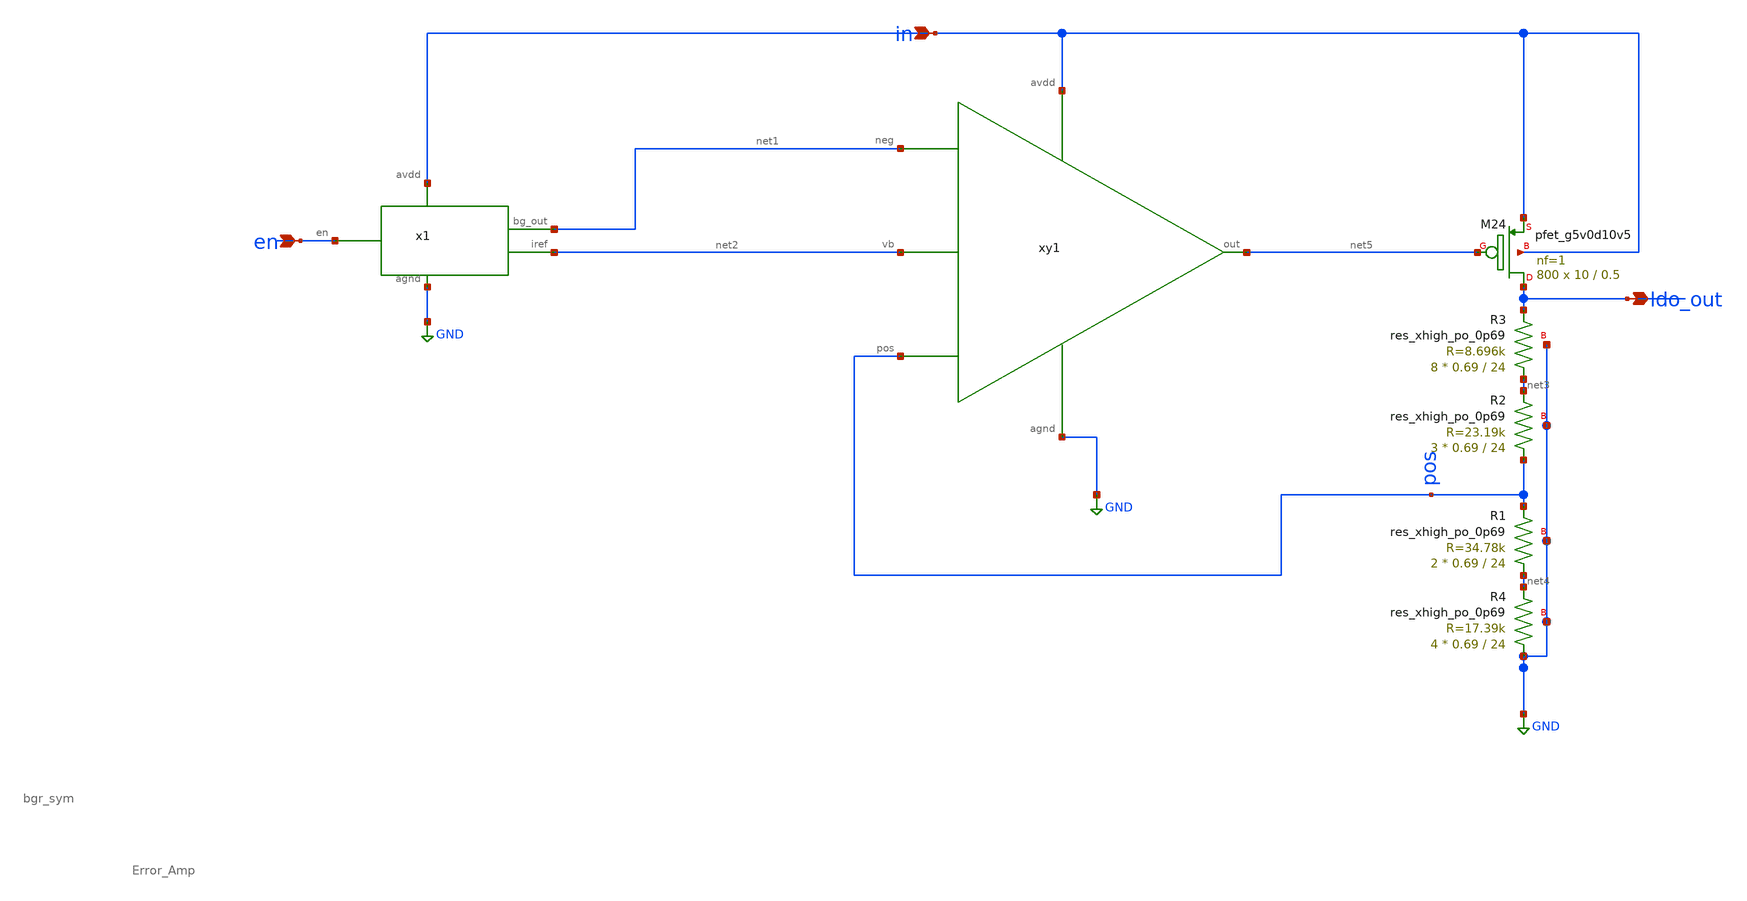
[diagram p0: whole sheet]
** sch_path: xschem/ldo_v1/ldo_v1_lvs.sch
**.subckt ldo_v1_lvs in en ldo_out
*.ipin in
*.ipin en
*.opin ldo_out
x1 in net1 GND net2 en bgr_sym
xy1 net1 pos net2 net5 in GND Error_Amp
XM24 ldo_out net5 in in sky130_fd_pr__pfet_g5v0d10v5 L=0.5 W=10 nf=1 ad='int((nf+1)/2) * W/nf * 0.29'
+ as='int((nf+2)/2) * W/nf * 0.29' pd='2*int((nf+1)/2) * (W/nf + 0.29)' ps='2*int((nf+2)/2) * (W/nf + 0.29)'
+ nrd='0.29 / W' nrs='0.29 / W' sa=0 sb=0 sd=0 mult=800 m=800
XR2 pos net3 GND sky130_fd_pr__res_xhigh_po_0p69 L=24 mult=3 m=3
XR3 net3 ldo_out GND sky130_fd_pr__res_xhigh_po_0p69 L=24 mult=8 m=8
XR1 net4 pos GND sky130_fd_pr__res_xhigh_po_0p69 L=24 mult=2 m=2
XR4 GND net4 GND sky130_fd_pr__res_xhigh_po_0p69 L=24 mult=4 m=4
**.ends

* expanding   symbol:  bgr_sym.sym # of pins=5
** sym_path: xschem/ldo_v1/bgr_sym.sym
** sch_path: xschem/ldo_v1/bgr_sym.sch
.subckt bgr_sym avdd bg_out agnd iref en
*.iopin avdd
*.iopin agnd
*.opin bg_out
*.opin iref
*.iopin en
XM2 iref mir avdd avdd sky130_fd_pr__pfet_g5v0d10v5 L=2 W=3 nf=1 ad='int((nf+1)/2) * W/nf * 0.29' as='int((nf+2)/2) * W/nf * 0.29'
+ pd='2*int((nf+1)/2) * (W/nf + 0.29)' ps='2*int((nf+2)/2) * (W/nf + 0.29)' nrd='0.29 / W' nrs='0.29 / W'
+ sa=0 sb=0 sd=0 mult=4 m=4
XM1 inn mir avdd avdd sky130_fd_pr__pfet_g5v0d10v5 L=2 W=3 nf=1 ad='int((nf+1)/2) * W/nf * 0.29' as='int((nf+2)/2) * W/nf * 0.29'
+ pd='2*int((nf+1)/2) * (W/nf + 0.29)' ps='2*int((nf+2)/2) * (W/nf + 0.29)' nrd='0.29 / W' nrs='0.29 / W'
+ sa=0 sb=0 sd=0 mult=8 m=8
XM3 inp mir avdd avdd sky130_fd_pr__pfet_g5v0d10v5 L=2 W=3 nf=1 ad='int((nf+1)/2) * W/nf * 0.29' as='int((nf+2)/2) * W/nf * 0.29'
+ pd='2*int((nf+1)/2) * (W/nf + 0.29)' ps='2*int((nf+2)/2) * (W/nf + 0.29)' nrd='0.29 / W' nrs='0.29 / W'
+ sa=0 sb=0 sd=0 mult=8 m=8
XM4 bg_out mir avdd avdd sky130_fd_pr__pfet_g5v0d10v5 L=2 W=3 nf=1 ad='int((nf+1)/2) * W/nf * 0.29' as='int((nf+2)/2) * W/nf * 0.29'
+ pd='2*int((nf+1)/2) * (W/nf + 0.29)' ps='2*int((nf+2)/2) * (W/nf + 0.29)' nrd='0.29 / W' nrs='0.29 / W'
+ sa=0 sb=0 sd=0 mult=8 m=8
XQ1 agnd agnd net2 sky130_fd_pr__pnp_05v5_W0p68L0p68 m=1
XQ5 agnd agnd net1 sky130_fd_pr__pnp_05v5_W0p68L0p68 m=1
XQ6 agnd agnd net1 sky130_fd_pr__pnp_05v5_W0p68L0p68 m=1
XQ7 agnd agnd net1 sky130_fd_pr__pnp_05v5_W0p68L0p68 m=1
XQ9 agnd agnd net1 sky130_fd_pr__pnp_05v5_W0p68L0p68 m=1
XQ11 agnd agnd net1 sky130_fd_pr__pnp_05v5_W0p68L0p68 m=1
XQ13 agnd agnd net1 sky130_fd_pr__pnp_05v5_W0p68L0p68 m=1
XQ15 agnd agnd net1 sky130_fd_pr__pnp_05v5_W0p68L0p68 m=1
XQ17 agnd agnd net1 sky130_fd_pr__pnp_05v5_W0p68L0p68 m=1
XM8 net4 net4 avdd avdd sky130_fd_pr__pfet_g5v0d10v5 L=2 W=3 nf=1 ad='int((nf+1)/2) * W/nf * 0.29' as='int((nf+2)/2) * W/nf * 0.29'
+ pd='2*int((nf+1)/2) * (W/nf + 0.29)' ps='2*int((nf+2)/2) * (W/nf + 0.29)' nrd='0.29 / W' nrs='0.29 / W'
+ sa=0 sb=0 sd=0 mult=4 m=4
XM12 net4 inp net3 agnd sky130_fd_pr__nfet_g5v0d10v5 L=1 W=3 nf=1 ad='int((nf+1)/2) * W/nf * 0.29' as='int((nf+2)/2) * W/nf * 0.29'
+ pd='2*int((nf+1)/2) * (W/nf + 0.29)' ps='2*int((nf+2)/2) * (W/nf + 0.29)' nrd='0.29 / W' nrs='0.29 / W'
+ sa=0 sb=0 sd=0 mult=8 m=8
XM21 mir inn net3 agnd sky130_fd_pr__nfet_g5v0d10v5 L=1 W=3 nf=1 ad='int((nf+1)/2) * W/nf * 0.29' as='int((nf+2)/2) * W/nf * 0.29'
+ pd='2*int((nf+1)/2) * (W/nf + 0.29)' ps='2*int((nf+2)/2) * (W/nf + 0.29)' nrd='0.29 / W' nrs='0.29 / W'
+ sa=0 sb=0 sd=0 mult=8 m=8
XM23 mir net4 avdd avdd sky130_fd_pr__pfet_g5v0d10v5 L=2 W=3 nf=1 ad='int((nf+1)/2) * W/nf * 0.29' as='int((nf+2)/2) * W/nf * 0.29'
+ pd='2*int((nf+1)/2) * (W/nf + 0.29)' ps='2*int((nf+2)/2) * (W/nf + 0.29)' nrd='0.29 / W' nrs='0.29 / W'
+ sa=0 sb=0 sd=0 mult=4 m=4
XM15 net3 net5 agnd agnd sky130_fd_pr__nfet_g5v0d10v5 L=2 W=5 nf=1 ad='int((nf+1)/2) * W/nf * 0.29' as='int((nf+2)/2) * W/nf * 0.29'
+ pd='2*int((nf+1)/2) * (W/nf + 0.29)' ps='2*int((nf+2)/2) * (W/nf + 0.29)' nrd='0.29 / W' nrs='0.29 / W'
+ sa=0 sb=0 sd=0 mult=4 m=4
XM25 net5 mir avdd avdd sky130_fd_pr__pfet_g5v0d10v5 L=2 W=3 nf=1 ad='int((nf+1)/2) * W/nf * 0.29' as='int((nf+2)/2) * W/nf * 0.29'
+ pd='2*int((nf+1)/2) * (W/nf + 0.29)' ps='2*int((nf+2)/2) * (W/nf + 0.29)' nrd='0.29 / W' nrs='0.29 / W'
+ sa=0 sb=0 sd=0 mult=8 m=8
XM16 net5 net5 agnd agnd sky130_fd_pr__nfet_g5v0d10v5 L=2 W=5 nf=1 ad='int((nf+1)/2) * W/nf * 0.29' as='int((nf+2)/2) * W/nf * 0.29'
+ pd='2*int((nf+1)/2) * (W/nf + 0.29)' ps='2*int((nf+2)/2) * (W/nf + 0.29)' nrd='0.29 / W' nrs='0.29 / W'
+ sa=0 sb=0 sd=0 mult=4 m=4
XR1 net6 inp agnd sky130_fd_pr__res_xhigh_po_0p69 L=27 mult=3 m=3
XR2 net2 inn agnd sky130_fd_pr__res_xhigh_po_0p69 L=27 mult=3 m=3
XR10 net1 net6 agnd sky130_fd_pr__res_xhigh_po_0p69 L=27 mult=6 m=6
XR11 agnd net7 agnd sky130_fd_pr__res_xhigh_po_0p69 L=27 mult=15 m=15
XR6 net10 net6 agnd sky130_fd_pr__res_xhigh_po_0p69 L=27 mult=1 m=1
XR5 net11 bg_out agnd sky130_fd_pr__res_xhigh_po_0p69 L=27 mult=1 m=1
XM19 mir en avdd avdd sky130_fd_pr__pfet_g5v0d10v5 L=0.5 W=0.42 nf=1 ad='int((nf+1)/2) * W/nf * 0.29'
+ as='int((nf+2)/2) * W/nf * 0.29' pd='2*int((nf+1)/2) * (W/nf + 0.29)' ps='2*int((nf+2)/2) * (W/nf + 0.29)'
+ nrd='0.29 / W' nrs='0.29 / W' sa=0 sb=0 sd=0 mult=2 m=2
XC2 avdd mir sky130_fd_pr__cap_mim_m3_1 W=20 L=20 MF=1 m=1
XM5 net9 net9 avdd avdd sky130_fd_pr__pfet_g5v0d10v5 L=3 W=0.42 nf=1 ad='int((nf+1)/2) * W/nf * 0.29'
+ as='int((nf+2)/2) * W/nf * 0.29' pd='2*int((nf+1)/2) * (W/nf + 0.29)' ps='2*int((nf+2)/2) * (W/nf + 0.29)'
+ nrd='0.29 / W' nrs='0.29 / W' sa=0 sb=0 sd=0 mult=2 m=2
XM6 net8 net8 net9 avdd sky130_fd_pr__pfet_g5v0d10v5 L=3 W=0.42 nf=1 ad='int((nf+1)/2) * W/nf * 0.29'
+ as='int((nf+2)/2) * W/nf * 0.29' pd='2*int((nf+1)/2) * (W/nf + 0.29)' ps='2*int((nf+2)/2) * (W/nf + 0.29)'
+ nrd='0.29 / W' nrs='0.29 / W' sa=0 sb=0 sd=0 mult=2 m=2
XM7 net8 bg_out agnd agnd sky130_fd_pr__nfet_g5v0d10v5 L=2 W=0.42 nf=1 ad='int((nf+1)/2) * W/nf * 0.29'
+ as='int((nf+2)/2) * W/nf * 0.29' pd='2*int((nf+1)/2) * (W/nf + 0.29)' ps='2*int((nf+2)/2) * (W/nf + 0.29)'
+ nrd='0.29 / W' nrs='0.29 / W' sa=0 sb=0 sd=0 mult=2 m=2
XM9 mir net8 agnd agnd sky130_fd_pr__nfet_g5v0d10v5 L=0.5 W=5 nf=1 ad='int((nf+1)/2) * W/nf * 0.29' as='int((nf+2)/2) * W/nf * 0.29'
+ pd='2*int((nf+1)/2) * (W/nf + 0.29)' ps='2*int((nf+2)/2) * (W/nf + 0.29)' nrd='0.29 / W' nrs='0.29 / W'
+ sa=0 sb=0 sd=0 mult=4 m=4
XR3 agnd net10 agnd sky130_fd_pr__res_xhigh_po_0p69 L=27 mult=15 m=15
XR4 agnd net11 agnd sky130_fd_pr__res_xhigh_po_0p69 L=27 mult=53 m=53
XR7 net7 net2 agnd sky130_fd_pr__res_xhigh_po_0p69 L=27 mult=1 m=1
.ends


* expanding   symbol:  Error_Amp.sym # of pins=6
** sym_path: xschem/ldo_v1/Error_Amp.sym
** sch_path: xschem/ldo_v1/Error_Amp.sch
.subckt Error_Amp neg pos vb out avdd agnd
*.opin out
*.iopin avdd
*.iopin agnd
*.iopin vb
*.ipin neg
*.ipin pos
XM8 net2 net2 avdd avdd sky130_fd_pr__pfet_g5v0d10v5 L=1.2 W=3 nf=1 ad='int((nf+1)/2) * W/nf * 0.29'
+ as='int((nf+2)/2) * W/nf * 0.29' pd='2*int((nf+1)/2) * (W/nf + 0.29)' ps='2*int((nf+2)/2) * (W/nf + 0.29)'
+ nrd='0.29 / W' nrs='0.29 / W' sa=0 sb=0 sd=0 mult=4 m=4
XM9 net2 neg net3 agnd sky130_fd_pr__nfet_g5v0d10v5 L=1 W=2 nf=1 ad='int((nf+1)/2) * W/nf * 0.29' as='int((nf+2)/2) * W/nf * 0.29'
+ pd='2*int((nf+1)/2) * (W/nf + 0.29)' ps='2*int((nf+2)/2) * (W/nf + 0.29)' nrd='0.29 / W' nrs='0.29 / W'
+ sa=0 sb=0 sd=0 mult=8 m=8
XM10 net1 pos net3 agnd sky130_fd_pr__nfet_g5v0d10v5 L=1 W=2 nf=1 ad='int((nf+1)/2) * W/nf * 0.29' as='int((nf+2)/2) * W/nf * 0.29'
+ pd='2*int((nf+1)/2) * (W/nf + 0.29)' ps='2*int((nf+2)/2) * (W/nf + 0.29)' nrd='0.29 / W' nrs='0.29 / W'
+ sa=0 sb=0 sd=0 mult=8 m=8
XM11 net1 net2 avdd avdd sky130_fd_pr__pfet_g5v0d10v5 L=1.2 W=3 nf=1 ad='int((nf+1)/2) * W/nf * 0.29'
+ as='int((nf+2)/2) * W/nf * 0.29' pd='2*int((nf+1)/2) * (W/nf + 0.29)' ps='2*int((nf+2)/2) * (W/nf + 0.29)'
+ nrd='0.29 / W' nrs='0.29 / W' sa=0 sb=0 sd=0 mult=4 m=4
XM13 net3 vb agnd agnd sky130_fd_pr__nfet_g5v0d10v5 L=1 W=1 nf=1 ad='int((nf+1)/2) * W/nf * 0.29' as='int((nf+2)/2) * W/nf * 0.29'
+ pd='2*int((nf+1)/2) * (W/nf + 0.29)' ps='2*int((nf+2)/2) * (W/nf + 0.29)' nrd='0.29 / W' nrs='0.29 / W'
+ sa=0 sb=0 sd=0 mult=8 m=8
XM14 out net1 avdd avdd sky130_fd_pr__pfet_g5v0d10v5 L=1.2 W=3 nf=1 ad='int((nf+1)/2) * W/nf * 0.29'
+ as='int((nf+2)/2) * W/nf * 0.29' pd='2*int((nf+1)/2) * (W/nf + 0.29)' ps='2*int((nf+2)/2) * (W/nf + 0.29)'
+ nrd='0.29 / W' nrs='0.29 / W' sa=0 sb=0 sd=0 mult=12 m=12
XM18 out vb agnd agnd sky130_fd_pr__nfet_g5v0d10v5 L=1 W=1 nf=1 ad='int((nf+1)/2) * W/nf * 0.29' as='int((nf+2)/2) * W/nf * 0.29'
+ pd='2*int((nf+1)/2) * (W/nf + 0.29)' ps='2*int((nf+2)/2) * (W/nf + 0.29)' nrd='0.29 / W' nrs='0.29 / W'
+ sa=0 sb=0 sd=0 mult=12 m=12
XC3 net1 net4 sky130_fd_pr__cap_mim_m3_1 W=50 L=50 MF=1 m=1
XR7 out net4 agnd sky130_fd_pr__res_xhigh_po_0p69 L=4.5 mult=1 m=1
XM20 vb vb agnd agnd sky130_fd_pr__nfet_g5v0d10v5 L=1 W=1 nf=1 ad='int((nf+1)/2) * W/nf * 0.29' as='int((nf+2)/2) * W/nf * 0.29'
+ pd='2*int((nf+1)/2) * (W/nf + 0.29)' ps='2*int((nf+2)/2) * (W/nf + 0.29)' nrd='0.29 / W' nrs='0.29 / W'
+ sa=0 sb=0 sd=0 mult=4 m=4
.ends

.GLOBAL GND
.end
